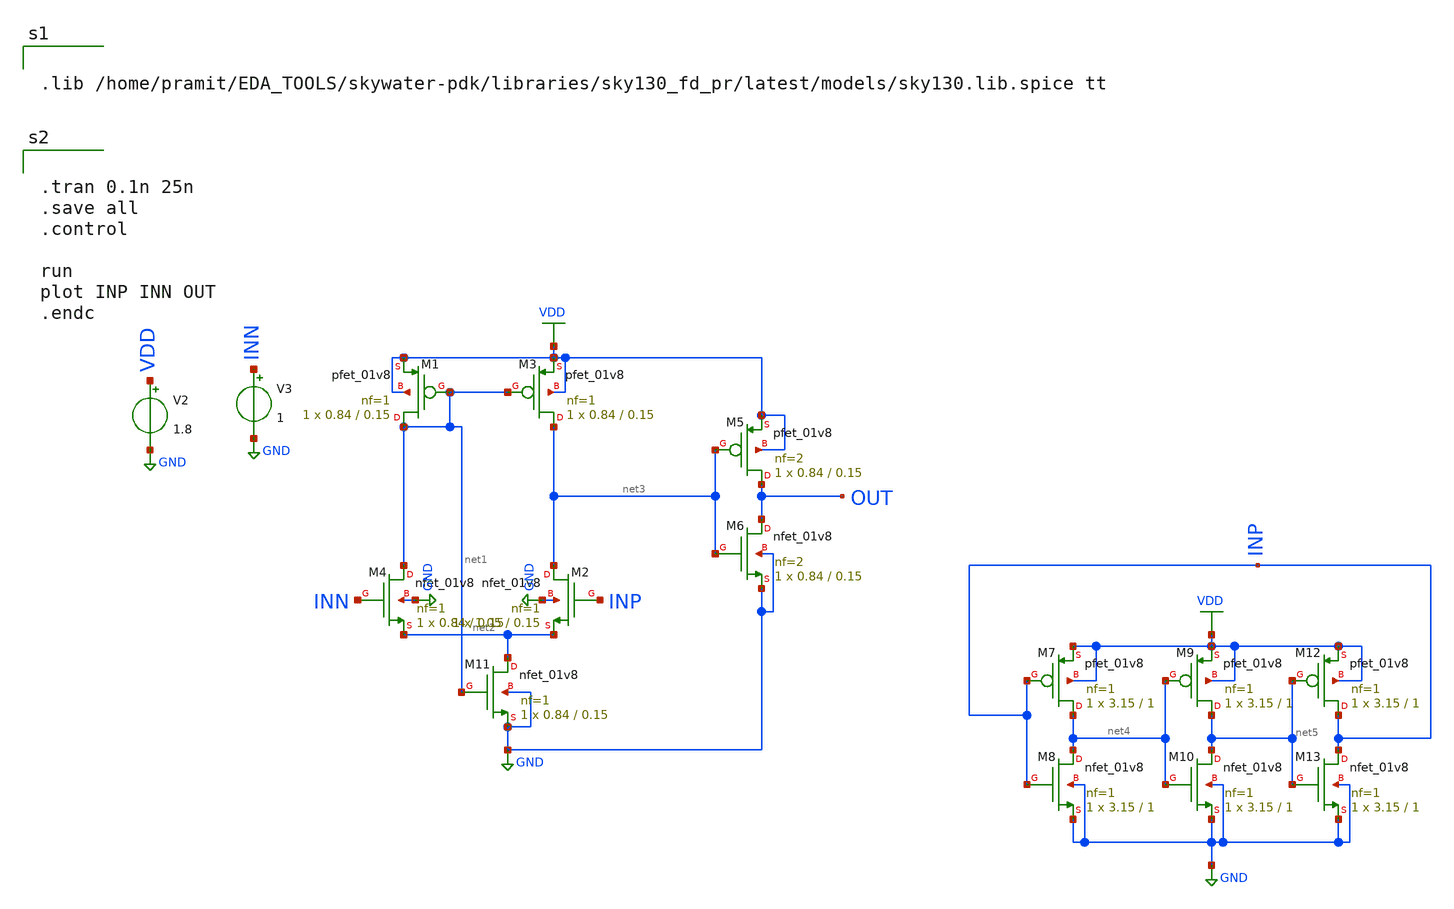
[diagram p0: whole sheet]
** sch_path: week5/ADC_layout/1bit_adc.sch
**.subckt 1bit_adc
XM1 net1 net1 VDD VDD sky130_fd_pr__pfet_01v8 L=0.15 W=0.84 nf=1 ad='int((nf+1)/2) * W/nf * 0.29' as='int((nf+2)/2) * W/nf * 0.29'
+ pd='2*int((nf+1)/2) * (W/nf + 0.29)' ps='2*int((nf+2)/2) * (W/nf + 0.29)' nrd='0.29 / W' nrs='0.29 / W'
+ sa=0 sb=0 sd=0 mult=1 m=1
XM2 net3 INP net2 GND sky130_fd_pr__nfet_01v8 L=0.15 W=1.05 nf=1 ad='int((nf+1)/2) * W/nf * 0.29' as='int((nf+2)/2) * W/nf * 0.29'
+ pd='2*int((nf+1)/2) * (W/nf + 0.29)' ps='2*int((nf+2)/2) * (W/nf + 0.29)' nrd='0.29 / W' nrs='0.29 / W'
+ sa=0 sb=0 sd=0 mult=1 m=1
XM3 net3 net1 VDD VDD sky130_fd_pr__pfet_01v8 L=0.15 W=0.84 nf=1 ad='int((nf+1)/2) * W/nf * 0.29' as='int((nf+2)/2) * W/nf * 0.29'
+ pd='2*int((nf+1)/2) * (W/nf + 0.29)' ps='2*int((nf+2)/2) * (W/nf + 0.29)' nrd='0.29 / W' nrs='0.29 / W'
+ sa=0 sb=0 sd=0 mult=1 m=1
XM4 net1 INN net2 GND sky130_fd_pr__nfet_01v8 L=0.15 W=0.84 nf=1 ad='int((nf+1)/2) * W/nf * 0.29' as='int((nf+2)/2) * W/nf * 0.29'
+ pd='2*int((nf+1)/2) * (W/nf + 0.29)' ps='2*int((nf+2)/2) * (W/nf + 0.29)' nrd='0.29 / W' nrs='0.29 / W'
+ sa=0 sb=0 sd=0 mult=1 m=1
XM11 net2 net1 GND GND sky130_fd_pr__nfet_01v8 L=0.15 W=0.84 nf=1 ad='int((nf+1)/2) * W/nf * 0.29' as='int((nf+2)/2) * W/nf * 0.29'
+ pd='2*int((nf+1)/2) * (W/nf + 0.29)' ps='2*int((nf+2)/2) * (W/nf + 0.29)' nrd='0.29 / W' nrs='0.29 / W'
+ sa=0 sb=0 sd=0 mult=1 m=1
V2 VDD GND 1.8
V3 INN GND 1
XM5 OUT net3 VDD VDD sky130_fd_pr__pfet_01v8 L=0.15 W=0.84 nf=2 ad='int((nf+1)/2) * W/nf * 0.29' as='int((nf+2)/2) * W/nf * 0.29'
+ pd='2*int((nf+1)/2) * (W/nf + 0.29)' ps='2*int((nf+2)/2) * (W/nf + 0.29)' nrd='0.29 / W' nrs='0.29 / W'
+ sa=0 sb=0 sd=0 mult=1 m=1
XM6 OUT net3 GND GND sky130_fd_pr__nfet_01v8 L=0.15 W=0.84 nf=2 ad='int((nf+1)/2) * W/nf * 0.29' as='int((nf+2)/2) * W/nf * 0.29'
+ pd='2*int((nf+1)/2) * (W/nf + 0.29)' ps='2*int((nf+2)/2) * (W/nf + 0.29)' nrd='0.29 / W' nrs='0.29 / W'
+ sa=0 sb=0 sd=0 mult=1 m=1
XM7 net4 INP VDD VDD sky130_fd_pr__pfet_01v8 L=1 W=3.15 nf=1 ad='int((nf+1)/2) * W/nf * 0.29' as='int((nf+2)/2) * W/nf * 0.29'
+ pd='2*int((nf+1)/2) * (W/nf + 0.29)' ps='2*int((nf+2)/2) * (W/nf + 0.29)' nrd='0.29 / W' nrs='0.29 / W'
+ sa=0 sb=0 sd=0 mult=1 m=1
XM8 net4 INP GND GND sky130_fd_pr__nfet_01v8 L=1 W=3.15 nf=1 ad='int((nf+1)/2) * W/nf * 0.29' as='int((nf+2)/2) * W/nf * 0.29'
+ pd='2*int((nf+1)/2) * (W/nf + 0.29)' ps='2*int((nf+2)/2) * (W/nf + 0.29)' nrd='0.29 / W' nrs='0.29 / W'
+ sa=0 sb=0 sd=0 mult=1 m=1
XM9 net5 net4 VDD VDD sky130_fd_pr__pfet_01v8 L=1 W=3.15 nf=1 ad='int((nf+1)/2) * W/nf * 0.29' as='int((nf+2)/2) * W/nf * 0.29'
+ pd='2*int((nf+1)/2) * (W/nf + 0.29)' ps='2*int((nf+2)/2) * (W/nf + 0.29)' nrd='0.29 / W' nrs='0.29 / W'
+ sa=0 sb=0 sd=0 mult=1 m=1
XM10 net5 net4 GND GND sky130_fd_pr__nfet_01v8 L=1 W=3.15 nf=1 ad='int((nf+1)/2) * W/nf * 0.29' as='int((nf+2)/2) * W/nf * 0.29'
+ pd='2*int((nf+1)/2) * (W/nf + 0.29)' ps='2*int((nf+2)/2) * (W/nf + 0.29)' nrd='0.29 / W' nrs='0.29 / W'
+ sa=0 sb=0 sd=0 mult=1 m=1
XM12 INP net5 VDD VDD sky130_fd_pr__pfet_01v8 L=1 W=3.15 nf=1 ad='int((nf+1)/2) * W/nf * 0.29' as='int((nf+2)/2) * W/nf * 0.29'
+ pd='2*int((nf+1)/2) * (W/nf + 0.29)' ps='2*int((nf+2)/2) * (W/nf + 0.29)' nrd='0.29 / W' nrs='0.29 / W'
+ sa=0 sb=0 sd=0 mult=1 m=1
XM13 INP net5 GND GND sky130_fd_pr__nfet_01v8 L=1 W=3.15 nf=1 ad='int((nf+1)/2) * W/nf * 0.29' as='int((nf+2)/2) * W/nf * 0.29'
+ pd='2*int((nf+1)/2) * (W/nf + 0.29)' ps='2*int((nf+2)/2) * (W/nf + 0.29)' nrd='0.29 / W' nrs='0.29 / W'
+ sa=0 sb=0 sd=0 mult=1 m=1
**** begin user architecture code


.lib /home/pramit/EDA_TOOLS/skywater-pdk/libraries/sky130_fd_pr/latest/models/sky130.lib.spice tt



.tran 0.1n 25n
.save all
.control

run
plot INP INN OUT
.endc

**** end user architecture code
**.ends
.GLOBAL VDD
.GLOBAL GND
.end
